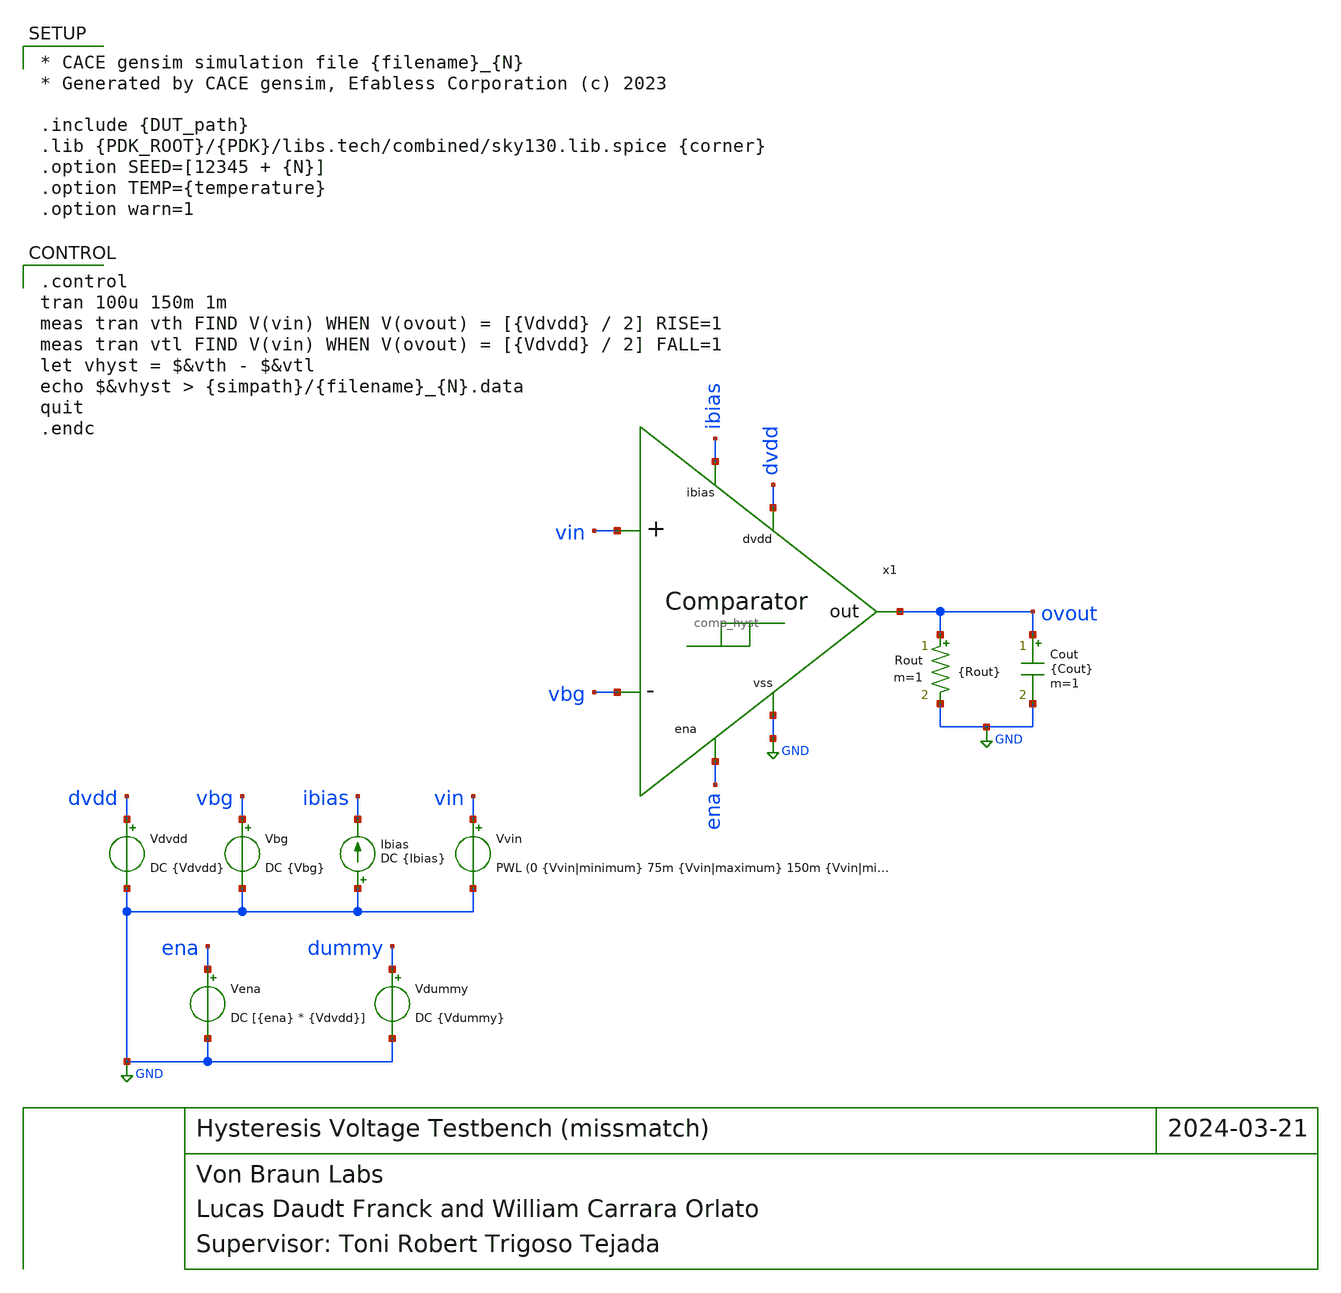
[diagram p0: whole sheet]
** sch_path: blocks/comp_hyst/cace/tb_vhyst_mm.sch
**.subckt tb_vhyst_mm
Vdvdd dvdd GND DC {Vdvdd}
Vbg vbg GND DC {Vbg}
Ibias GND ibias DC {Ibias}
Vena ena GND DC [{ena} * {Vdvdd}]
Vdummy dummy GND DC {Vdummy}
Vvin vin GND PWL (0 {Vvin|minimum} 75m {Vvin|maximum} 150m {Vvin|minimum})
Cout ovout GND {Cout} m=1
Rout ovout GND {Rout} m=1
x1 dvdd ovout vbg vin ena ibias GND comp_hyst
**** begin user architecture code

* CACE gensim simulation file {filename}_{N}
* Generated by CACE gensim, Efabless Corporation (c) 2023

.include {DUT_path}
.lib {PDK_ROOT}/{PDK}/libs.tech/combined/sky130.lib.spice {corner}
.option SEED=[12345 + {N}]
.option TEMP={temperature}
.option warn=1


.control
tran 100u 150m 1m
meas tran vth FIND V(vin) WHEN V(ovout) = [{Vdvdd} / 2] RISE=1
meas tran vtl FIND V(vin) WHEN V(ovout) = [{Vdvdd} / 2] FALL=1
let vhyst = $&vth - $&vtl
echo $&vhyst > {simpath}/{filename}_{N}.data
quit
.endc


**** end user architecture code
**.ends

* expanding   symbol:  /home/vblabs/Music/blocks/comp_hyst/xschem/comp_hyst.sym # of pins=7
** sym_path: blocks/comp_hyst/xschem/comp_hyst.sym
** sch_path: blocks/comp_hyst/xschem/comp_hyst.sch
.subckt comp_hyst dvdd out vref vin ena ibias vss
*.iopin dvdd
*.ipin vref
*.ipin vin
*.opin out
*.ipin ibias
*.ipin ena
*.iopin vss
XM6 net3 net4 dvdd dvdd sky130_fd_pr__pfet_01v8 L=8 W=1 nf=1 ad='int((nf+1)/2) * W/nf * 0.29' as='int((nf+2)/2) * W/nf * 0.29'
+ pd='2*int((nf+1)/2) * (W/nf + 0.29)' ps='2*int((nf+2)/2) * (W/nf + 0.29)' nrd='0.29 / W' nrs='0.29 / W'
+ sa=0 sb=0 sd=0 mult=1 m=1
XM7 net4 net4 dvdd dvdd sky130_fd_pr__pfet_01v8 L=8 W=1 nf=1 ad='int((nf+1)/2) * W/nf * 0.29' as='int((nf+2)/2) * W/nf * 0.29'
+ pd='2*int((nf+1)/2) * (W/nf + 0.29)' ps='2*int((nf+2)/2) * (W/nf + 0.29)' nrd='0.29 / W' nrs='0.29 / W'
+ sa=0 sb=0 sd=0 mult=1 m=1
XM8 net2 net4 dvdd dvdd sky130_fd_pr__pfet_01v8 L=8 W=1 nf=1 ad='int((nf+1)/2) * W/nf * 0.29' as='int((nf+2)/2) * W/nf * 0.29'
+ pd='2*int((nf+1)/2) * (W/nf + 0.29)' ps='2*int((nf+2)/2) * (W/nf + 0.29)' nrd='0.29 / W' nrs='0.29 / W'
+ sa=0 sb=0 sd=0 mult=1 m=1
XM10 net3 net3 dvdd dvdd sky130_fd_pr__pfet_01v8 L=16 W=1 nf=1 ad='int((nf+1)/2) * W/nf * 0.29' as='int((nf+2)/2) * W/nf * 0.29'
+ pd='2*int((nf+1)/2) * (W/nf + 0.29)' ps='2*int((nf+2)/2) * (W/nf + 0.29)' nrd='0.29 / W' nrs='0.29 / W'
+ sa=0 sb=0 sd=0 mult=1 m=1
XM11 ibias ibias vss vss sky130_fd_pr__nfet_01v8 L=20 W=1 nf=1 ad='int((nf+1)/2) * W/nf * 0.29' as='int((nf+2)/2) * W/nf * 0.29'
+ pd='2*int((nf+1)/2) * (W/nf + 0.29)' ps='2*int((nf+2)/2) * (W/nf + 0.29)' nrd='0.29 / W' nrs='0.29 / W'
+ sa=0 sb=0 sd=0 mult=1 m=1
XM12 net1 ibias vss vss sky130_fd_pr__nfet_01v8 L=20 W=1 nf=1 ad='int((nf+1)/2) * W/nf * 0.29' as='int((nf+2)/2) * W/nf * 0.29'
+ pd='2*int((nf+1)/2) * (W/nf + 0.29)' ps='2*int((nf+2)/2) * (W/nf + 0.29)' nrd='0.29 / W' nrs='0.29 / W'
+ sa=0 sb=0 sd=0 mult=1 m=1
XM4 out net3 dvdd dvdd sky130_fd_pr__pfet_01v8 L=1 W=3 nf=1 ad='int((nf+1)/2) * W/nf * 0.29' as='int((nf+2)/2) * W/nf * 0.29'
+ pd='2*int((nf+1)/2) * (W/nf + 0.29)' ps='2*int((nf+2)/2) * (W/nf + 0.29)' nrd='0.29 / W' nrs='0.29 / W'
+ sa=0 sb=0 sd=0 mult=1 m=1
XM13 out net2 vss vss sky130_fd_pr__nfet_01v8 L=1 W=3 nf=1 ad='int((nf+1)/2) * W/nf * 0.29' as='int((nf+2)/2) * W/nf * 0.29'
+ pd='2*int((nf+1)/2) * (W/nf + 0.29)' ps='2*int((nf+2)/2) * (W/nf + 0.29)' nrd='0.29 / W' nrs='0.29 / W'
+ sa=0 sb=0 sd=0 mult=1 m=1
XM20 out ena_b vss vss sky130_fd_pr__nfet_01v8 L=3 W=1 nf=1 ad='int((nf+1)/2) * W/nf * 0.29' as='int((nf+2)/2) * W/nf * 0.29'
+ pd='2*int((nf+1)/2) * (W/nf + 0.29)' ps='2*int((nf+2)/2) * (W/nf + 0.29)' nrd='0.29 / W' nrs='0.29 / W'
+ sa=0 sb=0 sd=0 mult=1 m=1
XM3[0] net4 vref net1 vss sky130_fd_pr__nfet_g5v0d10v5 L=10 W=2 nf=1 ad='int((nf+1)/2) * W/nf * 0.29'
+ as='int((nf+2)/2) * W/nf * 0.29' pd='2*int((nf+1)/2) * (W/nf + 0.29)' ps='2*int((nf+2)/2) * (W/nf + 0.29)'
+ nrd='0.29 / W' nrs='0.29 / W' sa=0 sb=0 sd=0 mult=1 m=1
XM3[1] net4 vref net1 vss sky130_fd_pr__nfet_g5v0d10v5 L=10 W=2 nf=1 ad='int((nf+1)/2) * W/nf * 0.29'
+ as='int((nf+2)/2) * W/nf * 0.29' pd='2*int((nf+1)/2) * (W/nf + 0.29)' ps='2*int((nf+2)/2) * (W/nf + 0.29)'
+ nrd='0.29 / W' nrs='0.29 / W' sa=0 sb=0 sd=0 mult=1 m=1
XM3[2] net4 vref net1 vss sky130_fd_pr__nfet_g5v0d10v5 L=10 W=2 nf=1 ad='int((nf+1)/2) * W/nf * 0.29'
+ as='int((nf+2)/2) * W/nf * 0.29' pd='2*int((nf+1)/2) * (W/nf + 0.29)' ps='2*int((nf+2)/2) * (W/nf + 0.29)'
+ nrd='0.29 / W' nrs='0.29 / W' sa=0 sb=0 sd=0 mult=1 m=1
XM3[3] net4 vref net1 vss sky130_fd_pr__nfet_g5v0d10v5 L=10 W=2 nf=1 ad='int((nf+1)/2) * W/nf * 0.29'
+ as='int((nf+2)/2) * W/nf * 0.29' pd='2*int((nf+1)/2) * (W/nf + 0.29)' ps='2*int((nf+2)/2) * (W/nf + 0.29)'
+ nrd='0.29 / W' nrs='0.29 / W' sa=0 sb=0 sd=0 mult=1 m=1
XM4[0] net3 vin net1 vss sky130_fd_pr__nfet_g5v0d10v5 L=10 W=2 nf=1 ad='int((nf+1)/2) * W/nf * 0.29'
+ as='int((nf+2)/2) * W/nf * 0.29' pd='2*int((nf+1)/2) * (W/nf + 0.29)' ps='2*int((nf+2)/2) * (W/nf + 0.29)'
+ nrd='0.29 / W' nrs='0.29 / W' sa=0 sb=0 sd=0 mult=1 m=1
XM4[1] net3 vin net1 vss sky130_fd_pr__nfet_g5v0d10v5 L=10 W=2 nf=1 ad='int((nf+1)/2) * W/nf * 0.29'
+ as='int((nf+2)/2) * W/nf * 0.29' pd='2*int((nf+1)/2) * (W/nf + 0.29)' ps='2*int((nf+2)/2) * (W/nf + 0.29)'
+ nrd='0.29 / W' nrs='0.29 / W' sa=0 sb=0 sd=0 mult=1 m=1
XM4[2] net3 vin net1 vss sky130_fd_pr__nfet_g5v0d10v5 L=10 W=2 nf=1 ad='int((nf+1)/2) * W/nf * 0.29'
+ as='int((nf+2)/2) * W/nf * 0.29' pd='2*int((nf+1)/2) * (W/nf + 0.29)' ps='2*int((nf+2)/2) * (W/nf + 0.29)'
+ nrd='0.29 / W' nrs='0.29 / W' sa=0 sb=0 sd=0 mult=1 m=1
XM4[3] net3 vin net1 vss sky130_fd_pr__nfet_g5v0d10v5 L=10 W=2 nf=1 ad='int((nf+1)/2) * W/nf * 0.29'
+ as='int((nf+2)/2) * W/nf * 0.29' pd='2*int((nf+1)/2) * (W/nf + 0.29)' ps='2*int((nf+2)/2) * (W/nf + 0.29)'
+ nrd='0.29 / W' nrs='0.29 / W' sa=0 sb=0 sd=0 mult=1 m=1
XM3 ibias ena_b vss vss sky130_fd_pr__nfet_01v8 L=3 W=1 nf=1 ad='int((nf+1)/2) * W/nf * 0.29' as='int((nf+2)/2) * W/nf * 0.29'
+ pd='2*int((nf+1)/2) * (W/nf + 0.29)' ps='2*int((nf+2)/2) * (W/nf + 0.29)' nrd='0.29 / W' nrs='0.29 / W'
+ sa=0 sb=0 sd=0 mult=1 m=1
XM1[0] net4 net3 dvdd dvdd sky130_fd_pr__pfet_01v8 L=16 W=1.4 nf=1 ad='int((nf+1)/2) * W/nf * 0.29' as='int((nf+2)/2) * W/nf * 0.29'
+ pd='2*int((nf+1)/2) * (W/nf + 0.29)' ps='2*int((nf+2)/2) * (W/nf + 0.29)' nrd='0.29 / W' nrs='0.29 / W'
+ sa=0 sb=0 sd=0 mult=1 m=1
XM1[1] net4 net3 dvdd dvdd sky130_fd_pr__pfet_01v8 L=16 W=1.4 nf=1 ad='int((nf+1)/2) * W/nf * 0.29' as='int((nf+2)/2) * W/nf * 0.29'
+ pd='2*int((nf+1)/2) * (W/nf + 0.29)' ps='2*int((nf+2)/2) * (W/nf + 0.29)' nrd='0.29 / W' nrs='0.29 / W'
+ sa=0 sb=0 sd=0 mult=1 m=1
XM9 net2 net2 vss vss sky130_fd_pr__nfet_01v8 L=8 W=1 nf=1 ad='int((nf+1)/2) * W/nf * 0.29' as='int((nf+2)/2) * W/nf * 0.29'
+ pd='2*int((nf+1)/2) * (W/nf + 0.29)' ps='2*int((nf+2)/2) * (W/nf + 0.29)' nrd='0.29 / W' nrs='0.29 / W'
+ sa=0 sb=0 sd=0 mult=1 m=1
XM5 net3 ena dvdd dvdd sky130_fd_pr__pfet_01v8 L=3 W=1 nf=1 ad='int((nf+1)/2) * W/nf * 0.29' as='int((nf+2)/2) * W/nf * 0.29'
+ pd='2*int((nf+1)/2) * (W/nf + 0.29)' ps='2*int((nf+2)/2) * (W/nf + 0.29)' nrd='0.29 / W' nrs='0.29 / W'
+ sa=0 sb=0 sd=0 mult=1 m=1
XM14 net4 ena dvdd dvdd sky130_fd_pr__pfet_01v8 L=3 W=1 nf=1 ad='int((nf+1)/2) * W/nf * 0.29' as='int((nf+2)/2) * W/nf * 0.29'
+ pd='2*int((nf+1)/2) * (W/nf + 0.29)' ps='2*int((nf+2)/2) * (W/nf + 0.29)' nrd='0.29 / W' nrs='0.29 / W'
+ sa=0 sb=0 sd=0 mult=1 m=1
XM15 net2 ena_b vss vss sky130_fd_pr__nfet_01v8 L=3 W=1 nf=1 ad='int((nf+1)/2) * W/nf * 0.29' as='int((nf+2)/2) * W/nf * 0.29'
+ pd='2*int((nf+1)/2) * (W/nf + 0.29)' ps='2*int((nf+2)/2) * (W/nf + 0.29)' nrd='0.29 / W' nrs='0.29 / W'
+ sa=0 sb=0 sd=0 mult=1 m=1
XM1 ena_b ena dvdd dvdd sky130_fd_pr__pfet_01v8 L=8 W=1 nf=1 ad='int((nf+1)/2) * W/nf * 0.29' as='int((nf+2)/2) * W/nf * 0.29'
+ pd='2*int((nf+1)/2) * (W/nf + 0.29)' ps='2*int((nf+2)/2) * (W/nf + 0.29)' nrd='0.29 / W' nrs='0.29 / W'
+ sa=0 sb=0 sd=0 mult=1 m=1
XM2 ena_b ena vss vss sky130_fd_pr__nfet_01v8 L=8 W=1 nf=1 ad='int((nf+1)/2) * W/nf * 0.29' as='int((nf+2)/2) * W/nf * 0.29'
+ pd='2*int((nf+1)/2) * (W/nf + 0.29)' ps='2*int((nf+2)/2) * (W/nf + 0.29)' nrd='0.29 / W' nrs='0.29 / W'
+ sa=0 sb=0 sd=0 mult=1 m=1
.ends

.GLOBAL GND
.end
